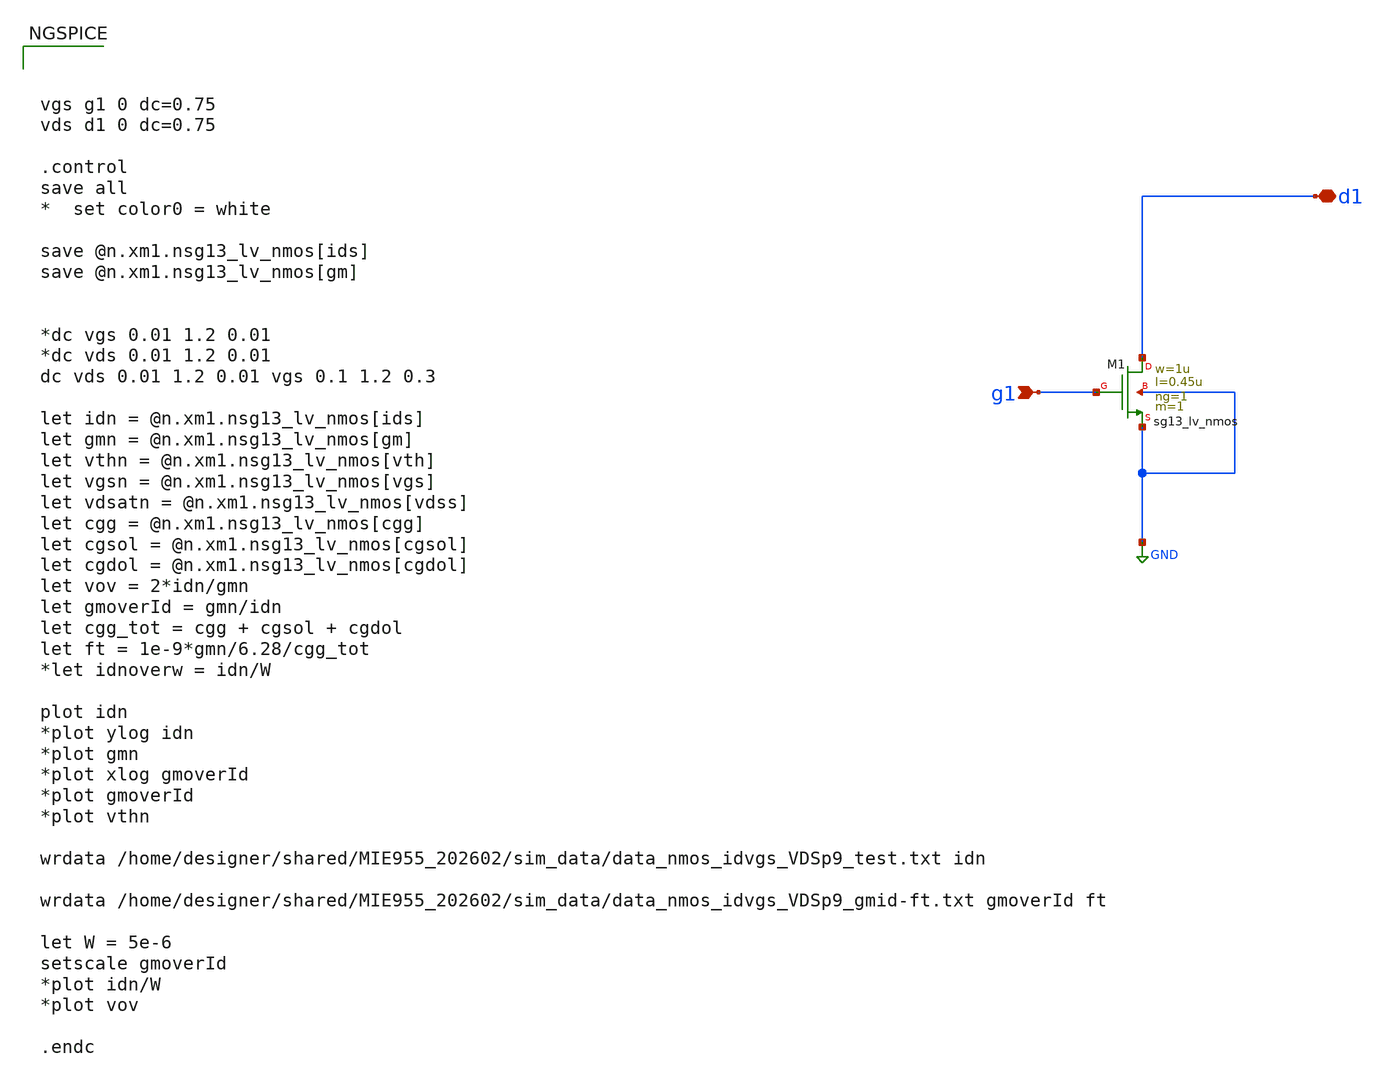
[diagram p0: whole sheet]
** sch_path: xschem/Tareas/Tarea_1/nmoslv_charac_MIE955-202602-HW1.sch
**.subckt nmoslv_charac_MIE955-202602-HW1 g1 d1
*.ipin g1
*.iopin d1
XM1 d1 g1 GND GND sg13_lv_nmos w=1u l=0.45u ng=1 m=1 mm_ok=1
**** begin user architecture code



vgs g1 0 dc=0.75
vds d1 0 dc=0.75

.control
save all
*  set color0 = white

save @n.xm1.nsg13_lv_nmos[ids]
save @n.xm1.nsg13_lv_nmos[gm]


*dc vgs 0.01 1.2 0.01
*dc vds 0.01 1.2 0.01
dc vds 0.01 1.2 0.01 vgs 0.1 1.2 0.3

let idn = @n.xm1.nsg13_lv_nmos[ids]
let gmn = @n.xm1.nsg13_lv_nmos[gm]
let vthn = @n.xm1.nsg13_lv_nmos[vth]
let vgsn = @n.xm1.nsg13_lv_nmos[vgs]
let vdsatn = @n.xm1.nsg13_lv_nmos[vdss]
let cgg = @n.xm1.nsg13_lv_nmos[cgg]
let cgsol = @n.xm1.nsg13_lv_nmos[cgsol]
let cgdol = @n.xm1.nsg13_lv_nmos[cgdol]
let vov = 2*idn/gmn
let gmoverId = gmn/idn
let cgg_tot = cgg + cgsol + cgdol
let ft = 1e-9*gmn/6.28/cgg_tot
*let idnoverw = idn/W

plot idn
*plot ylog idn
*plot gmn
*plot xlog gmoverId
*plot gmoverId
*plot vthn

wrdata /home/designer/shared/MIE955_202602/sim_data/data_nmos_idvgs_VDSp9_test.txt idn

wrdata /home/designer/shared/MIE955_202602/sim_data/data_nmos_idvgs_VDSp9_gmid-ft.txt gmoverId ft

let W = 5e-6
setscale gmoverId
*plot idn/W
*plot vov

.endc




.lib cornerMOShv.lib mos_tt
.lib cornerMOSlv.lib mos_tt
*.lib cornerMOShv.lib mos_ff
*.lib cornerMOSlv.lib mos_ff
*.lib cornerMOShv.lib mos_ss
*.lib cornerMOSlv.lib mos_ss
*.lib cornerMOShv.lib mos_sf
*.lib cornerMOSlv.lib mos_sf
*.lib cornerMOShv.lib mos_fs
*.lib cornerMOSlv.lib mos_fs

.include /opt/pdks/ihp-sg13g2/libs.ref/sg13g2_stdcell/spice/sg13g2_stdcell.spice
.lib $::SG13G2_MODELS/cornerRES.lib res_typ
.lib $::SG13G2_MODELS/cornerCAP.lib cap_typ
*.lib $::SG13G2_MODELS/diodes.lib

**** end user architecture code
**.ends
.GLOBAL GND
.end
